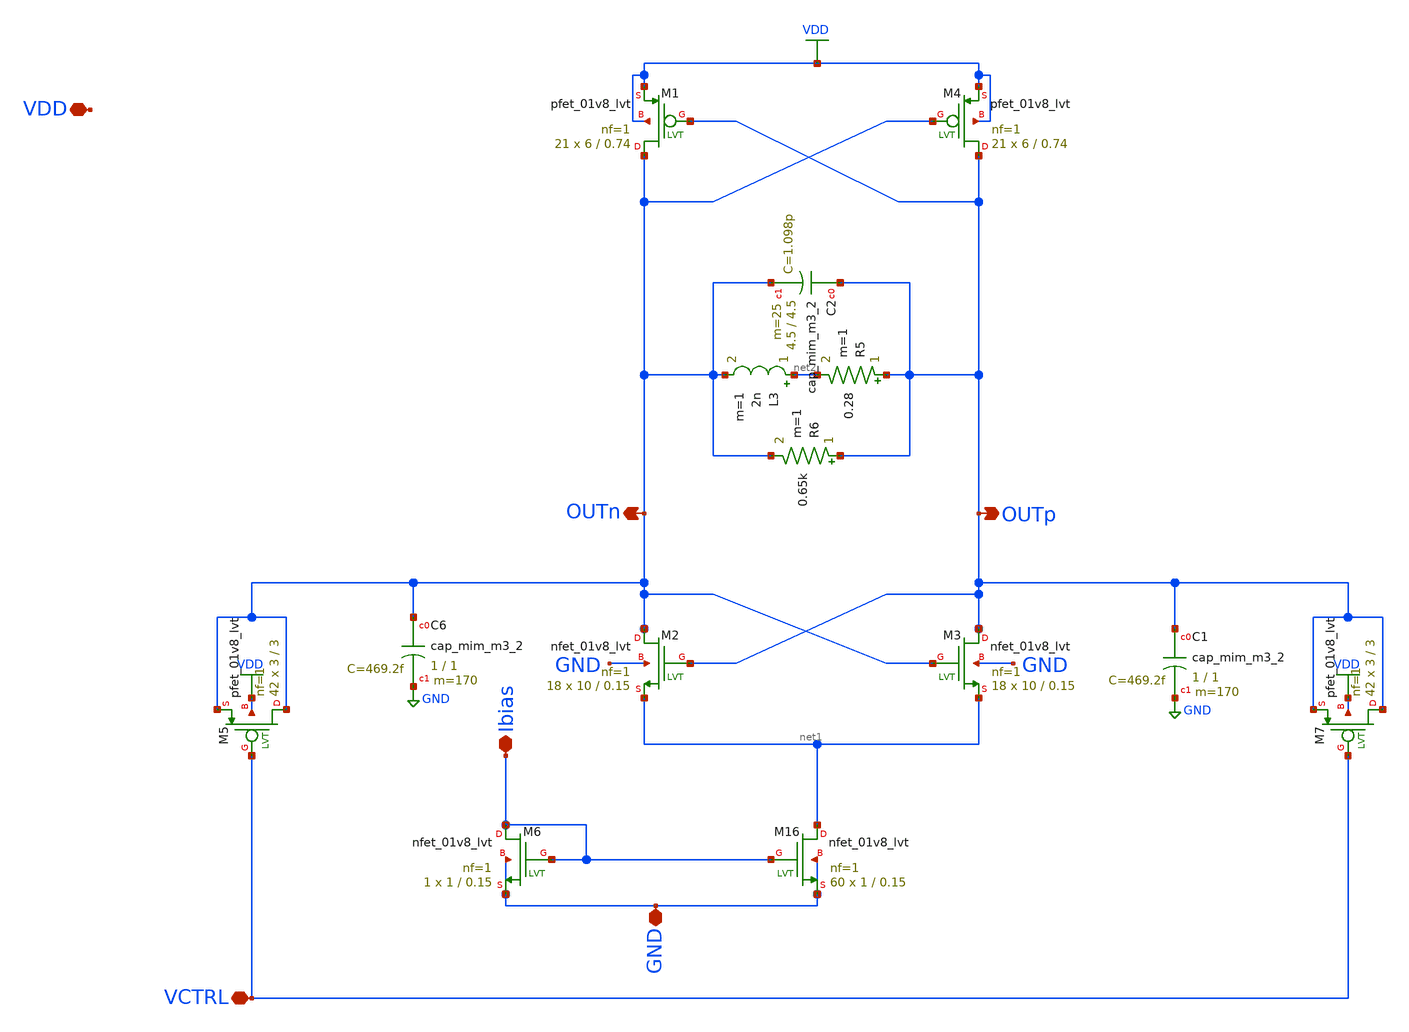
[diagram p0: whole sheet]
** sch_path: schematic/blocks/lc-vco/LC_VCO.sch
**.subckt LC_VCO VDD OUTp OUTn GND VCTRL Ibias
*.iopin VDD
*.opin OUTp
*.opin OUTn
*.iopin GND
*.iopin VCTRL
*.iopin Ibias
XM2 OUTn OUTp net1 GND sky130_fd_pr__nfet_01v8_lvt L=0.15 W=10 nf=1 ad='int((nf+1)/2) * W/nf * 0.29'
+ as='int((nf+2)/2) * W/nf * 0.29' pd='2*int((nf+1)/2) * (W/nf + 0.29)' ps='2*int((nf+2)/2) * (W/nf + 0.29)'
+ nrd='0.29 / W' nrs='0.29 / W' sa=0 sb=0 sd=0 mult=18 m=18
XM3 OUTp OUTn net1 GND sky130_fd_pr__nfet_01v8_lvt L=0.15 W=10 nf=1 ad='int((nf+1)/2) * W/nf * 0.29'
+ as='int((nf+2)/2) * W/nf * 0.29' pd='2*int((nf+1)/2) * (W/nf + 0.29)' ps='2*int((nf+2)/2) * (W/nf + 0.29)'
+ nrd='0.29 / W' nrs='0.29 / W' sa=0 sb=0 sd=0 mult=18 m=18
XM6 Ibias Ibias GND GND sky130_fd_pr__nfet_01v8_lvt L=0.15 W=1 nf=1 ad='int((nf+1)/2) * W/nf * 0.29'
+ as='int((nf+2)/2) * W/nf * 0.29' pd='2*int((nf+1)/2) * (W/nf + 0.29)' ps='2*int((nf+2)/2) * (W/nf + 0.29)'
+ nrd='0.29 / W' nrs='0.29 / W' sa=0 sb=0 sd=0 mult=1 m=1
XM16 net1 Ibias GND GND sky130_fd_pr__nfet_01v8_lvt L=0.15 W=1 nf=1 ad='int((nf+1)/2) * W/nf * 0.29'
+ as='int((nf+2)/2) * W/nf * 0.29' pd='2*int((nf+1)/2) * (W/nf + 0.29)' ps='2*int((nf+2)/2) * (W/nf + 0.29)'
+ nrd='0.29 / W' nrs='0.29 / W' sa=0 sb=0 sd=0 mult=60 m=60
L3 net2 OUTn 2n m=1
R5 OUTp net2 0.28 m=1
R6 OUTp OUTn 0.65k m=1
XC2 OUTp OUTn sky130_fd_pr__cap_mim_m3_2 W=4.5 L=4.5 MF=25 m=25
XM4 OUTp OUTn VDD VDD sky130_fd_pr__pfet_01v8_lvt L=0.74 W=6 nf=1 ad='int((nf+1)/2) * W/nf * 0.29' as='int((nf+2)/2) * W/nf * 0.29'
+ pd='2*int((nf+1)/2) * (W/nf + 0.29)' ps='2*int((nf+2)/2) * (W/nf + 0.29)' nrd='0.29 / W' nrs='0.29 / W'
+ sa=0 sb=0 sd=0 mult=21 m=21
XM1 OUTn OUTp VDD VDD sky130_fd_pr__pfet_01v8_lvt L=0.74 W=6 nf=1 ad='int((nf+1)/2) * W/nf * 0.29' as='int((nf+2)/2) * W/nf * 0.29'
+ pd='2*int((nf+1)/2) * (W/nf + 0.29)' ps='2*int((nf+2)/2) * (W/nf + 0.29)' nrd='0.29 / W' nrs='0.29 / W'
+ sa=0 sb=0 sd=0 mult=21 m=21
XM5 OUTn VCTRL OUTn VDD sky130_fd_pr__pfet_01v8_lvt L=3 W=3 nf=1 ad='int((nf+1)/2) * W/nf * 0.29' as='int((nf+2)/2) * W/nf * 0.29'
+ pd='2*int((nf+1)/2) * (W/nf + 0.29)' ps='2*int((nf+2)/2) * (W/nf + 0.29)' nrd='0.29 / W' nrs='0.29 / W'
+ sa=0 sb=0 sd=0 mult=42 m=42
XC6 OUTn GND sky130_fd_pr__cap_mim_m3_2 W=1 L=1 MF=170 m=170
XM7 OUTp VCTRL OUTp VDD sky130_fd_pr__pfet_01v8_lvt L=3 W=3 nf=1 ad='int((nf+1)/2) * W/nf * 0.29' as='int((nf+2)/2) * W/nf * 0.29'
+ pd='2*int((nf+1)/2) * (W/nf + 0.29)' ps='2*int((nf+2)/2) * (W/nf + 0.29)' nrd='0.29 / W' nrs='0.29 / W'
+ sa=0 sb=0 sd=0 mult=42 m=42
XC1 OUTp GND sky130_fd_pr__cap_mim_m3_2 W=1 L=1 MF=170 m=170
**.ends
.GLOBAL VDD
.GLOBAL GND
.end
